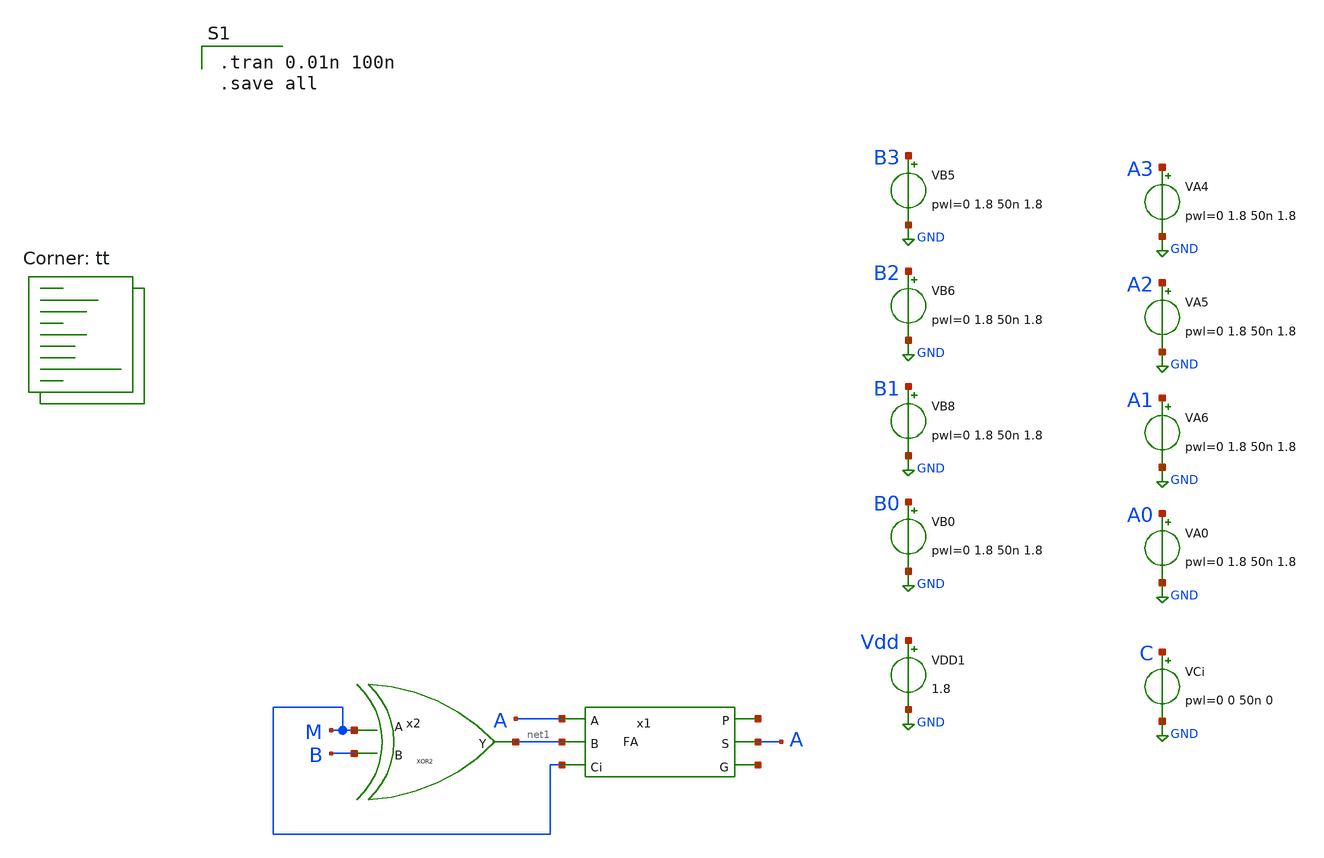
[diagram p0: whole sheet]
** sch_path: gates/1BITFASYMSUBADD.sch
**.subckt 1BITFASYMSUBADD
x1 net2 A net1 A M net3 FA
x2 M B net1 XOR2
VA4 A3 GND pwl=0 1.8 50n 1.8
VA5 A2 GND pwl=0 1.8 50n 1.8
VA6 A1 GND pwl=0 1.8 50n 1.8
VA0 A0 GND pwl=0 1.8 50n 1.8
VB5 B3 GND pwl=0 1.8 50n 1.8
VB6 B2 GND pwl=0 1.8 50n 1.8
VB8 B1 GND pwl=0 1.8 50n 1.8
VB0 B0 GND pwl=0 1.8 50n 1.8
VCi C GND pwl=0 0 50n 0
VDD1 Vdd GND 1.8
**** begin user architecture code

.tran 0.01n 100n
.save all

.lib $::SKYWATER_MODELS/sky130.lib.spice tt
**** end user architecture code
**.ends

* expanding   symbol:  FA.sym # of pins=6
** sym_path: gates/FA.sym
** sch_path: gates/FA.sch
.subckt FA P A B S Ci G
*.opin S
*.ipin A
*.ipin B
*.ipin Ci
*.opin P
*.opin G
x1 A B P XOR2
x2 P Ci S XOR2
x3 net1 Co G OR2
x4 Ci net1 P AND2
x5 A G B AND2
.ends


* expanding   symbol:  XOR2.sym # of pins=3
** sym_path: gates/XOR2.sym
** sch_path: gates/XOR2.sch
.subckt XOR2 B A Y
*.ipin A
*.ipin B
*.opin Y
XM1 Y A net5 GND sky130_fd_pr__nfet_01v8 L=0.15 W=1 nf=1 ad='int((nf+1)/2) * W/nf * 0.29' as='int((nf+2)/2) * W/nf * 0.29'
+ pd='2*int((nf+1)/2) * (W/nf + 0.29)' ps='2*int((nf+2)/2) * (W/nf + 0.29)' nrd='0.29 / W' nrs='0.29 / W'
+ sa=0 sb=0 sd=0 mult=1 m=1
XM2 net5 B GND GND sky130_fd_pr__nfet_01v8 L=0.15 W=1 nf=1 ad='int((nf+1)/2) * W/nf * 0.29' as='int((nf+2)/2) * W/nf * 0.29'
+ pd='2*int((nf+1)/2) * (W/nf + 0.29)' ps='2*int((nf+2)/2) * (W/nf + 0.29)' nrd='0.29 / W' nrs='0.29 / W'
+ sa=0 sb=0 sd=0 mult=1 m=1
XM3 Y net1 net2 VDD sky130_fd_pr__pfet_01v8 L=0.15 W=1 nf=1 ad='int((nf+1)/2) * W/nf * 0.29' as='int((nf+2)/2) * W/nf * 0.29'
+ pd='2*int((nf+1)/2) * (W/nf + 0.29)' ps='2*int((nf+2)/2) * (W/nf + 0.29)' nrd='0.29 / W' nrs='0.29 / W'
+ sa=0 sb=0 sd=0 mult=1 m=1
XM4 net2 A VDD VDD sky130_fd_pr__pfet_01v8 L=0.15 W=1 nf=1 ad='int((nf+1)/2) * W/nf * 0.29' as='int((nf+2)/2) * W/nf * 0.29'
+ pd='2*int((nf+1)/2) * (W/nf + 0.29)' ps='2*int((nf+2)/2) * (W/nf + 0.29)' nrd='0.29 / W' nrs='0.29 / W'
+ sa=0 sb=0 sd=0 mult=1 m=1
XM5 net2 B VDD VDD sky130_fd_pr__pfet_01v8 L=0.15 W=1 nf=1 ad='int((nf+1)/2) * W/nf * 0.29' as='int((nf+2)/2) * W/nf * 0.29'
+ pd='2*int((nf+1)/2) * (W/nf + 0.29)' ps='2*int((nf+2)/2) * (W/nf + 0.29)' nrd='0.29 / W' nrs='0.29 / W'
+ sa=0 sb=0 sd=0 mult=1 m=1
XM6 Y net3 net2 VDD sky130_fd_pr__pfet_01v8 L=0.15 W=1 nf=1 ad='int((nf+1)/2) * W/nf * 0.29' as='int((nf+2)/2) * W/nf * 0.29'
+ pd='2*int((nf+1)/2) * (W/nf + 0.29)' ps='2*int((nf+2)/2) * (W/nf + 0.29)' nrd='0.29 / W' nrs='0.29 / W'
+ sa=0 sb=0 sd=0 mult=1 m=1
XM7 Y net1 net4 GND sky130_fd_pr__nfet_01v8 L=0.15 W=1 nf=1 ad='int((nf+1)/2) * W/nf * 0.29' as='int((nf+2)/2) * W/nf * 0.29'
+ pd='2*int((nf+1)/2) * (W/nf + 0.29)' ps='2*int((nf+2)/2) * (W/nf + 0.29)' nrd='0.29 / W' nrs='0.29 / W'
+ sa=0 sb=0 sd=0 mult=1 m=1
XM8 net4 net3 GND GND sky130_fd_pr__nfet_01v8 L=0.15 W=1 nf=1 ad='int((nf+1)/2) * W/nf * 0.29' as='int((nf+2)/2) * W/nf * 0.29'
+ pd='2*int((nf+1)/2) * (W/nf + 0.29)' ps='2*int((nf+2)/2) * (W/nf + 0.29)' nrd='0.29 / W' nrs='0.29 / W'
+ sa=0 sb=0 sd=0 mult=1 m=1
X1 A net1 inv_vtc
X2 B net3 inv_vtc
.ends


* expanding   symbol:  OR2.sym # of pins=3
** sym_path: gates/OR2.sym
** sch_path: gates/OR2.sch
.subckt OR2 B Y A
*.ipin A
*.ipin B
*.opin Y
XM7 VDD B net2 VDD sky130_fd_pr__pfet_01v8 L=0.15 W=1 nf=1 ad='int((nf+1)/2) * W/nf * 0.29' as='int((nf+2)/2) * W/nf * 0.29'
+ pd='2*int((nf+1)/2) * (W/nf + 0.29)' ps='2*int((nf+2)/2) * (W/nf + 0.29)' nrd='0.29 / W' nrs='0.29 / W'
+ sa=0 sb=0 sd=0 mult=1 m=1
XM8 GND B net1 GND sky130_fd_pr__nfet_01v8 L=0.15 W=1 nf=1 ad='int((nf+1)/2) * W/nf * 0.29' as='int((nf+2)/2) * W/nf * 0.29'
+ pd='2*int((nf+1)/2) * (W/nf + 0.29)' ps='2*int((nf+2)/2) * (W/nf + 0.29)' nrd='0.29 / W' nrs='0.29 / W'
+ sa=0 sb=0 sd=0 mult=1 m=1
XM9 net2 A net1 VDD sky130_fd_pr__pfet_01v8 L=0.15 W=1 nf=1 ad='int((nf+1)/2) * W/nf * 0.29' as='int((nf+2)/2) * W/nf * 0.29'
+ pd='2*int((nf+1)/2) * (W/nf + 0.29)' ps='2*int((nf+2)/2) * (W/nf + 0.29)' nrd='0.29 / W' nrs='0.29 / W'
+ sa=0 sb=0 sd=0 mult=1 m=1
XM10 GND A net1 GND sky130_fd_pr__nfet_01v8 L=0.15 W=1 nf=1 ad='int((nf+1)/2) * W/nf * 0.29' as='int((nf+2)/2) * W/nf * 0.29'
+ pd='2*int((nf+1)/2) * (W/nf + 0.29)' ps='2*int((nf+2)/2) * (W/nf + 0.29)' nrd='0.29 / W' nrs='0.29 / W'
+ sa=0 sb=0 sd=0 mult=1 m=1
X1 net1 Y inv_vtc
.ends


* expanding   symbol:  AND2.sym # of pins=3
** sym_path: gates/AND2.sym
** sch_path: gates/AND2.sch
.subckt AND2 A Y B
*.opin Y
*.ipin A
*.ipin B
x1 A net1 B NAND2_Gate
X2 net1 Y inv_vtc
.ends


* expanding   symbol:  inv_vtc.sym # of pins=2
** sym_path: gates/inv_vtc.sym
** sch_path: gates/inv_vtc.sch
.subckt inv_vtc A Y
*.ipin A
*.opin Y
XM1 Y A VDD VDD sky130_fd_pr__pfet_01v8 L=0.15 W=2 nf=1 ad='int((nf+1)/2) * W/nf * 0.29' as='int((nf+2)/2) * W/nf * 0.29'
+ pd='2*int((nf+1)/2) * (W/nf + 0.29)' ps='2*int((nf+2)/2) * (W/nf + 0.29)' nrd='0.29 / W' nrs='0.29 / W'
+ sa=0 sb=0 sd=0 mult=1 m=1
XM2 Y A GND GND sky130_fd_pr__nfet_01v8 L=0.15 W=1 nf=1 ad='int((nf+1)/2) * W/nf * 0.29' as='int((nf+2)/2) * W/nf * 0.29'
+ pd='2*int((nf+1)/2) * (W/nf + 0.29)' ps='2*int((nf+2)/2) * (W/nf + 0.29)' nrd='0.29 / W' nrs='0.29 / W'
+ sa=0 sb=0 sd=0 mult=1 m=1
.ends


* expanding   symbol:  NAND2_Gate.sym # of pins=3
** sym_path: gates/NAND2_Gate.sym
** sch_path: gates/NAND2_Gate.sch
.subckt NAND2_Gate A Y B
*.ipin A
*.ipin B
*.opin Y
XM1 Y A net1 GND sky130_fd_pr__nfet_01v8 L=0.15 W=1 nf=1 ad='int((nf+1)/2) * W/nf * 0.29' as='int((nf+2)/2) * W/nf * 0.29'
+ pd='2*int((nf+1)/2) * (W/nf + 0.29)' ps='2*int((nf+2)/2) * (W/nf + 0.29)' nrd='0.29 / W' nrs='0.29 / W'
+ sa=0 sb=0 sd=0 mult=1 m=1
XM2 net1 B GND GND sky130_fd_pr__nfet_01v8 L=0.15 W=1 nf=1 ad='int((nf+1)/2) * W/nf * 0.29' as='int((nf+2)/2) * W/nf * 0.29'
+ pd='2*int((nf+1)/2) * (W/nf + 0.29)' ps='2*int((nf+2)/2) * (W/nf + 0.29)' nrd='0.29 / W' nrs='0.29 / W'
+ sa=0 sb=0 sd=0 mult=1 m=1
XM3 Y A VDD VDD sky130_fd_pr__pfet_01v8 L=0.15 W=1 nf=1 ad='int((nf+1)/2) * W/nf * 0.29' as='int((nf+2)/2) * W/nf * 0.29'
+ pd='2*int((nf+1)/2) * (W/nf + 0.29)' ps='2*int((nf+2)/2) * (W/nf + 0.29)' nrd='0.29 / W' nrs='0.29 / W'
+ sa=0 sb=0 sd=0 mult=1 m=1
XM4 Y B VDD VDD sky130_fd_pr__pfet_01v8 L=0.15 W=1 nf=1 ad='int((nf+1)/2) * W/nf * 0.29' as='int((nf+2)/2) * W/nf * 0.29'
+ pd='2*int((nf+1)/2) * (W/nf + 0.29)' ps='2*int((nf+2)/2) * (W/nf + 0.29)' nrd='0.29 / W' nrs='0.29 / W'
+ sa=0 sb=0 sd=0 mult=1 m=1
.ends

.GLOBAL GND
.GLOBAL VDD
.end
